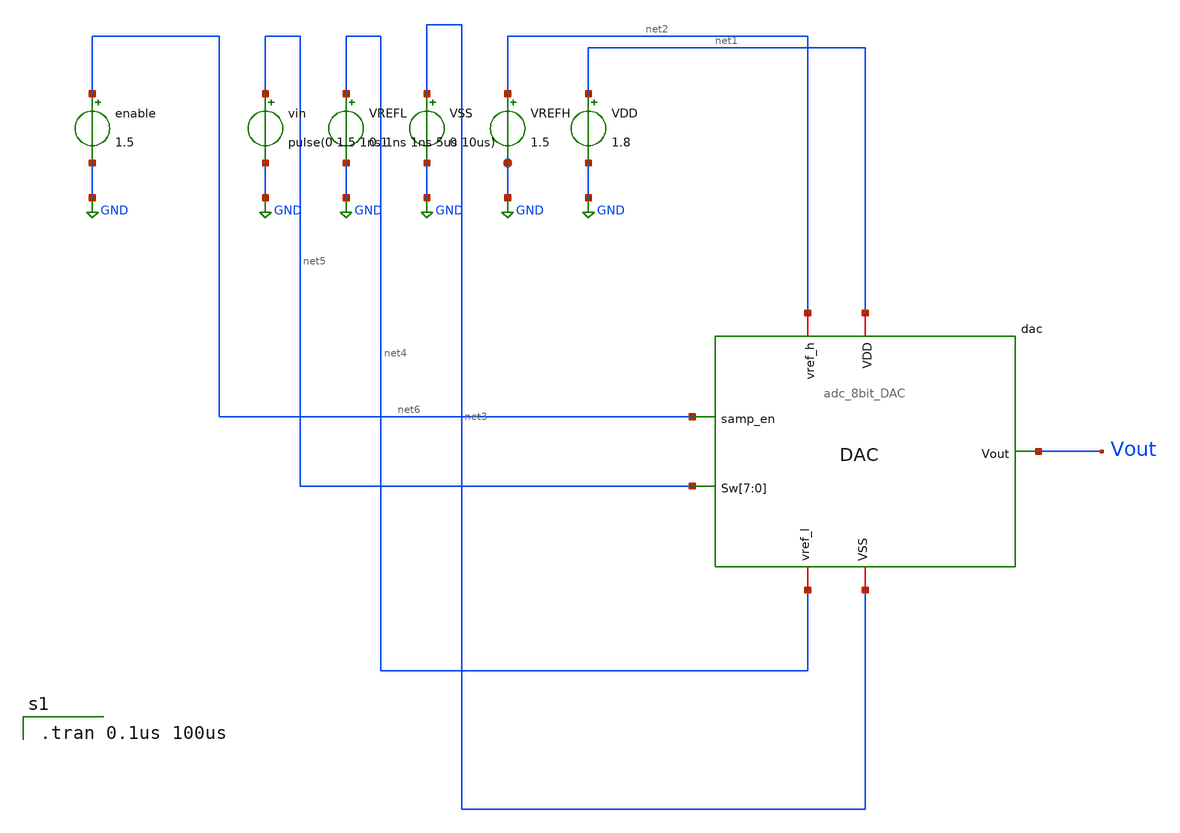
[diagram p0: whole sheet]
** sch_path: adc_8bit_DAC_tb.sch
**.subckt adc_8bit_DAC_tb
x1 Vout net3 net1 net2 net4 net5 net5 net5 net5 net5 net5 net5 net5 net6 adc_8bit_DAC
VDD net1 GND 1.8
VREFH net2 GND 1.5
VSS net3 GND 0
VREFL net4 GND 0.1
vin net5 GND pulse(0 1.5 1ns 1ns 1ns 5us 10us)
enable net6 GND 1.5
**** begin user architecture code

.tran 0.1us 100us


** opencircuitdesign pdks install
.lib $::SKYWATER_MODELS/sky130.lib.spice tt
.include $::SKYWATER_STDCELLS/sky130_fd_sc_hd.spice

**** end user architecture code
**.ends

* expanding   symbol:  adc_8bit_DAC.sym # of pins=7
** sym_path: adc_8bit_DAC.sym
** sch_path: adc_8bit_DAC.sch
.subckt adc_8bit_DAC Vout VSS VDD vref_h vref_l Sw[7] Sw[6] Sw[5] Sw[4] Sw[3] Sw[2] Sw[1] Sw[0]
+ samp_en
*.ipin Sw[7],Sw[6],Sw[5],Sw[4],Sw[3],Sw[2],Sw[1],Sw[0]
*.ipin samp_en
*.iopin VSS
*.iopin VDD
*.iopin vref_h
*.iopin vref_l
*.opin Vout
XM19 vref_h Sw[0] net8 VDD sky130_fd_pr__pfet_01v8 L=0.18 W=1.5 nf=1 ad='int((nf+1)/2) * W/nf * 0.29'
+ as='int((nf+2)/2) * W/nf * 0.29' pd='2*int((nf+1)/2) * (W/nf + 0.29)' ps='2*int((nf+2)/2) * (W/nf + 0.29)'
+ nrd='0.29 / W' nrs='0.29 / W' sa=0 sb=0 sd=0 mult=1 m=1
XM23 net8 Sw[0] vref_l VSS sky130_fd_pr__nfet_01v8 L=0.18 W=1.5 nf=2 ad='int((nf+1)/2) * W/nf * 0.29'
+ as='int((nf+2)/2) * W/nf * 0.29' pd='2*int((nf+1)/2) * (W/nf + 0.29)' ps='2*int((nf+2)/2) * (W/nf + 0.29)'
+ nrd='0.29 / W' nrs='0.29 / W' sa=0 sb=0 sd=0 mult=2 m=2
XM21 net6 Sw[2] vref_l VSS sky130_fd_pr__nfet_01v8 L=0.18 W=0.75 nf=4 ad='int((nf+1)/2) * W/nf * 0.29'
+ as='int((nf+2)/2) * W/nf * 0.29' pd='2*int((nf+1)/2) * (W/nf + 0.29)' ps='2*int((nf+2)/2) * (W/nf + 0.29)'
+ nrd='0.29 / W' nrs='0.29 / W' sa=0 sb=0 sd=0 mult=4 m=4
XM24 net7 Sw[1] vref_l VSS sky130_fd_pr__nfet_01v8 L=0.18 W=0.75 nf=4 ad='int((nf+1)/2) * W/nf * 0.29'
+ as='int((nf+2)/2) * W/nf * 0.29' pd='2*int((nf+1)/2) * (W/nf + 0.29)' ps='2*int((nf+2)/2) * (W/nf + 0.29)'
+ nrd='0.29 / W' nrs='0.29 / W' sa=0 sb=0 sd=0 mult=4 m=4
XM25 net5 Sw[3] vref_l VSS sky130_fd_pr__nfet_01v8 L=0.18 W=0.75 nf=6 ad='int((nf+1)/2) * W/nf * 0.29'
+ as='int((nf+2)/2) * W/nf * 0.29' pd='2*int((nf+1)/2) * (W/nf + 0.29)' ps='2*int((nf+2)/2) * (W/nf + 0.29)'
+ nrd='0.29 / W' nrs='0.29 / W' sa=0 sb=0 sd=0 mult=6 m=6
XM26 Vout samp_en vref_l VSS sky130_fd_pr__nfet_01v8 L=0.18 W=6 nf=12 ad='int((nf+1)/2) * W/nf * 0.29'
+ as='int((nf+2)/2) * W/nf * 0.29' pd='2*int((nf+1)/2) * (W/nf + 0.29)' ps='2*int((nf+2)/2) * (W/nf + 0.29)'
+ nrd='0.29 / W' nrs='0.29 / W' sa=0 sb=0 sd=0 mult=12 m=12
XM27 net1 Sw[4] vref_l VSS sky130_fd_pr__nfet_01v8 L=0.18 W=0.75 nf=12 ad='int((nf+1)/2) * W/nf * 0.29'
+ as='int((nf+2)/2) * W/nf * 0.29' pd='2*int((nf+1)/2) * (W/nf + 0.29)' ps='2*int((nf+2)/2) * (W/nf + 0.29)'
+ nrd='0.29 / W' nrs='0.29 / W' sa=0 sb=0 sd=0 mult=12 m=12
XM28 net2 Sw[5] vref_l VSS sky130_fd_pr__nfet_01v8 L=0.18 W=1.5 nf=12 ad='int((nf+1)/2) * W/nf * 0.29'
+ as='int((nf+2)/2) * W/nf * 0.29' pd='2*int((nf+1)/2) * (W/nf + 0.29)' ps='2*int((nf+2)/2) * (W/nf + 0.29)'
+ nrd='0.29 / W' nrs='0.29 / W' sa=0 sb=0 sd=0 mult=12 m=12
XM29 net3 Sw[6] vref_l VSS sky130_fd_pr__nfet_01v8 L=0.18 W=1.5 nf=24 ad='int((nf+1)/2) * W/nf * 0.29'
+ as='int((nf+2)/2) * W/nf * 0.29' pd='2*int((nf+1)/2) * (W/nf + 0.29)' ps='2*int((nf+2)/2) * (W/nf + 0.29)'
+ nrd='0.29 / W' nrs='0.29 / W' sa=0 sb=0 sd=0 mult=24 m=24
XM30 net4 Sw[7] vref_l VSS sky130_fd_pr__nfet_01v8 L=0.18 W=1.5 nf=48 ad='int((nf+1)/2) * W/nf * 0.29'
+ as='int((nf+2)/2) * W/nf * 0.29' pd='2*int((nf+1)/2) * (W/nf + 0.29)' ps='2*int((nf+2)/2) * (W/nf + 0.29)'
+ nrd='0.29 / W' nrs='0.29 / W' sa=0 sb=0 sd=0 mult=48 m=48
XM31 vref_h Sw[1] net7 VDD sky130_fd_pr__pfet_01v8 L=0.18 W=0.75 nf=2 ad='int((nf+1)/2) * W/nf * 0.29'
+ as='int((nf+2)/2) * W/nf * 0.29' pd='2*int((nf+1)/2) * (W/nf + 0.29)' ps='2*int((nf+2)/2) * (W/nf + 0.29)'
+ nrd='0.29 / W' nrs='0.29 / W' sa=0 sb=0 sd=0 mult=2 m=2
XM32 vref_h Sw[2] net6 VDD sky130_fd_pr__pfet_01v8 L=0.18 W=0.75 nf=2 ad='int((nf+1)/2) * W/nf * 0.29'
+ as='int((nf+2)/2) * W/nf * 0.29' pd='2*int((nf+1)/2) * (W/nf + 0.29)' ps='2*int((nf+2)/2) * (W/nf + 0.29)'
+ nrd='0.29 / W' nrs='0.29 / W' sa=0 sb=0 sd=0 mult=2 m=2
XM33 vref_h Sw[3] net5 VDD sky130_fd_pr__pfet_01v8 L=0.18 W=0.75 nf=3 ad='int((nf+1)/2) * W/nf * 0.29'
+ as='int((nf+2)/2) * W/nf * 0.29' pd='2*int((nf+1)/2) * (W/nf + 0.29)' ps='2*int((nf+2)/2) * (W/nf + 0.29)'
+ nrd='0.29 / W' nrs='0.29 / W' sa=0 sb=0 sd=0 mult=3 m=3
XM34 vref_h Sw[4] net1 VDD sky130_fd_pr__pfet_01v8 L=0.18 W=0.75 nf=6 ad='int((nf+1)/2) * W/nf * 0.29'
+ as='int((nf+2)/2) * W/nf * 0.29' pd='2*int((nf+1)/2) * (W/nf + 0.29)' ps='2*int((nf+2)/2) * (W/nf + 0.29)'
+ nrd='0.29 / W' nrs='0.29 / W' sa=0 sb=0 sd=0 mult=6 m=6
XM35 vref_h Sw[5] net2 VDD sky130_fd_pr__pfet_01v8 L=0.18 W=1.5 nf=6 ad='int((nf+1)/2) * W/nf * 0.29'
+ as='int((nf+2)/2) * W/nf * 0.29' pd='2*int((nf+1)/2) * (W/nf + 0.29)' ps='2*int((nf+2)/2) * (W/nf + 0.29)'
+ nrd='0.29 / W' nrs='0.29 / W' sa=0 sb=0 sd=0 mult=6 m=6
XM36 vref_h Sw[6] net3 VDD sky130_fd_pr__pfet_01v8 L=0.18 W=1.5 nf=12 ad='int((nf+1)/2) * W/nf * 0.29'
+ as='int((nf+2)/2) * W/nf * 0.29' pd='2*int((nf+1)/2) * (W/nf + 0.29)' ps='2*int((nf+2)/2) * (W/nf + 0.29)'
+ nrd='0.29 / W' nrs='0.29 / W' sa=0 sb=0 sd=0 mult=12 m=12
XM37 vref_h Sw[7] net4 VDD sky130_fd_pr__pfet_01v8 L=0.18 W=1.5 nf=24 ad='int((nf+1)/2) * W/nf * 0.29'
+ as='int((nf+2)/2) * W/nf * 0.29' pd='2*int((nf+1)/2) * (W/nf + 0.29)' ps='2*int((nf+2)/2) * (W/nf + 0.29)'
+ nrd='0.29 / W' nrs='0.29 / W' sa=0 sb=0 sd=0 mult=24 m=24
XC12 net9 net8 sky130_fd_pr__cap_mim_m3_1 W=1 L=1 MF=1 m=1
XC13 Vout net9 sky130_fd_pr__cap_mim_m3_1 W=1 L=1 MF=1 m=1
XC14 net10 vref_h sky130_fd_pr__cap_mim_m3_1 W=1 L=1 MF=1 m=1
XC15 Vout net10 sky130_fd_pr__cap_mim_m3_1 W=1 L=1 MF=1 m=1
XC16 Vout net7 sky130_fd_pr__cap_mim_m3_1 W=1 L=1 MF=1 m=1
XC17 Vout net6 sky130_fd_pr__cap_mim_m3_1 W=1 L=1 MF=1 m=1
XC18 Vout net5 sky130_fd_pr__cap_mim_m3_1 W=1 L=1 MF=1 m=1
XC19 Vout net1 sky130_fd_pr__cap_mim_m3_1 W=1 L=1 MF=1 m=1
XC20 Vout net2 sky130_fd_pr__cap_mim_m3_1 W=1 L=1 MF=1 m=1
XC21 Vout net3 sky130_fd_pr__cap_mim_m3_1 W=1 L=1 MF=1 m=1
XC22 Vout net4 sky130_fd_pr__cap_mim_m3_1 W=1 L=1 MF=1 m=1
**** begin user architecture code

.tran 0.1us 100us

**** end user architecture code
XM1 net11 net12 net13 VDD sky130_fd_pr__pfet_01v8_lvt L=0.15 W=1 nf=1 ad='int((nf+1)/2) * W/nf * 0.29'
+ as='int((nf+2)/2) * W/nf * 0.29' pd='2*int((nf+1)/2) * (W/nf + 0.29)' ps='2*int((nf+2)/2) * (W/nf + 0.29)'
+ nrd='0.29 / W' nrs='0.29 / W' sa=0 sb=0 sd=0 mult=1 m=1
XM2 net14 net15 net16 net17 sky130_fd_pr__pfet_01v8_hvt L=0.15 W='1 * 1 ' nf=1 ad='int((nf+1)/2) * W / nf * 0.29'
+ as='int((nf+2)/2) * W / nf * 0.29' pd='2*int((nf+1)/2) * (W / nf + 0.29)' ps='2*int((nf+2)/2) * (W / nf + 0.29)'
+ nrd='0.29 / W ' nrs='0.29 / W ' sa=0 sb=0 sd=0 mult=1 m=1
XM3 net18 net19 net20 net21 sky130_fd_pr__pfet_01v8_lvt L=0.35 W=1 nf=1 ad='int((nf+1)/2) * W/nf * 0.29'
+ as='int((nf+2)/2) * W/nf * 0.29' pd='2*int((nf+1)/2) * (W/nf + 0.29)' ps='2*int((nf+2)/2) * (W/nf + 0.29)'
+ nrd='0.29 / W' nrs='0.29 / W' sa=0 sb=0 sd=0 mult=1 m=1
.ends

.GLOBAL GND
.end
